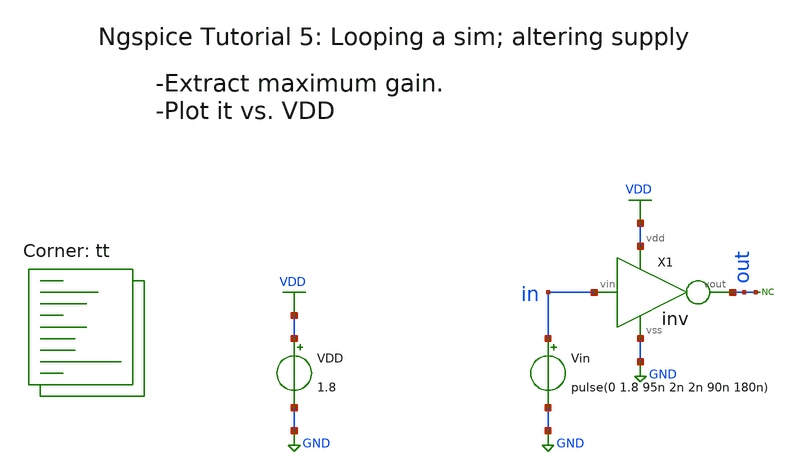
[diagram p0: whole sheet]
** sch_path: xsch/tut/ngspice_tut5.sch
**.subckt ngspice_tut5
Vin in GND pulse(0 1.8 95n 2n 2n 90n 180n)
VDD VDD GND 1.8
X1 in out VDD GND inv
* noconn out
**** begin user architecture code



* control language script

.control
let loops = 6							; number of loops, vector in plot 'const'
let vecmaxgain = vector(loops)							; vector in plot 'const'
let vecvdd = vector(loops)							; vector in plot 'const'
let vddd = 1.0							; supply voltage in plot 'const'
let index = 0							; loop index in plot 'const'

repeat $&loops							; loop start
	alter Vdd $&vddd						; alter the voltage Vdd
	dc vin 0 1.8 0.001						; run the dc sim
	let gain = deriv(v(out))						; calculate the gain
	let maxgain = vecmin(gain)						; find the maximum of the gain (min because gain is negative)
	let vecmaxgain[index] = maxgain						; store the corresponding max gain
	let vecvdd[index] = vddd						; store corresponding voltage
	let vddd = vddd + 0.2					        ; calculate the new voltage value for Vdd
	let index = index + 1						; raise the index
end

;destroy all							; delete all plot dc1 ..., no longer needed
plot dc1.v(out) dc2.v(out) dc3.v(out) dc4.v(out) dc5.v(out) dc6.v(out)
set xbrushwidth=2
set nolegend
plot vecmaxgain vs vecvdd xlabel 'Inverter supply voltage /V' ylabel 'Inverter gain V/V'
.endc

.end



.lib $::SKYWATER_MODELS/sky130.lib.spice tt
**** end user architecture code
**.ends
.GLOBAL VDD
.GLOBAL GND
.end
